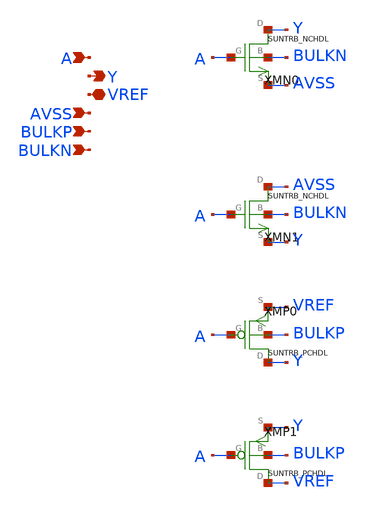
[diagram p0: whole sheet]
** sch_path: ip/sun_trb_sky130nm/design/SUN_TRB_SKY130NM/SUNTRB_SWX2_CV.sch
**.subckt SUNTRB_SWX2_CV A Y VREF AVSS BULKP BULKN
*.ipin A
*.opin Y
*.iopin VREF
*.ipin AVSS
*.ipin BULKP
*.ipin BULKN
XMN0 Y A AVSS BULKN SUNTRB_NCHDL xoffset=0 yoffset=0 angle=0
XMN1 AVSS A Y BULKN SUNTRB_NCHDL xoffset=0 yoffset=0 angle=0
XMP0 Y A VREF BULKP SUNTRB_PCHDL xoffset=0 yoffset=0 angle=0
XMP1 VREF A Y BULKP SUNTRB_PCHDL xoffset=0 yoffset=0 angle=0
**.ends
.end
